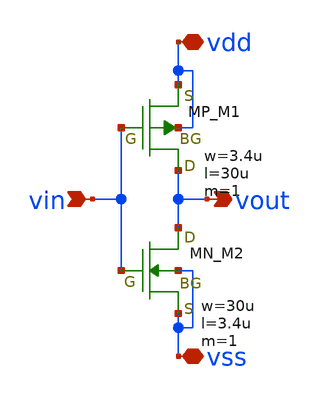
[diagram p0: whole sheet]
** sch_path: member_project/DCDC/ShuntaroOHNO/xschem/inverter_startup.sch
**.subckt inverter_startup vdd vss vin vout
*.iopin vdd
*.iopin vss
*.ipin vin
*.opin vout
XM1 vout vin vdd vdd PMOS w=3.4u l=30u as=0 ad=0 ps=0 pd=0 nrd=0 nrs=0 m=1
XM2 vout vin vss vss NMOS w=30u l=3.4u as=0 ad=0 ps=0 pd=0 nrd=0 nrs=0 m=1
**.ends
.end
